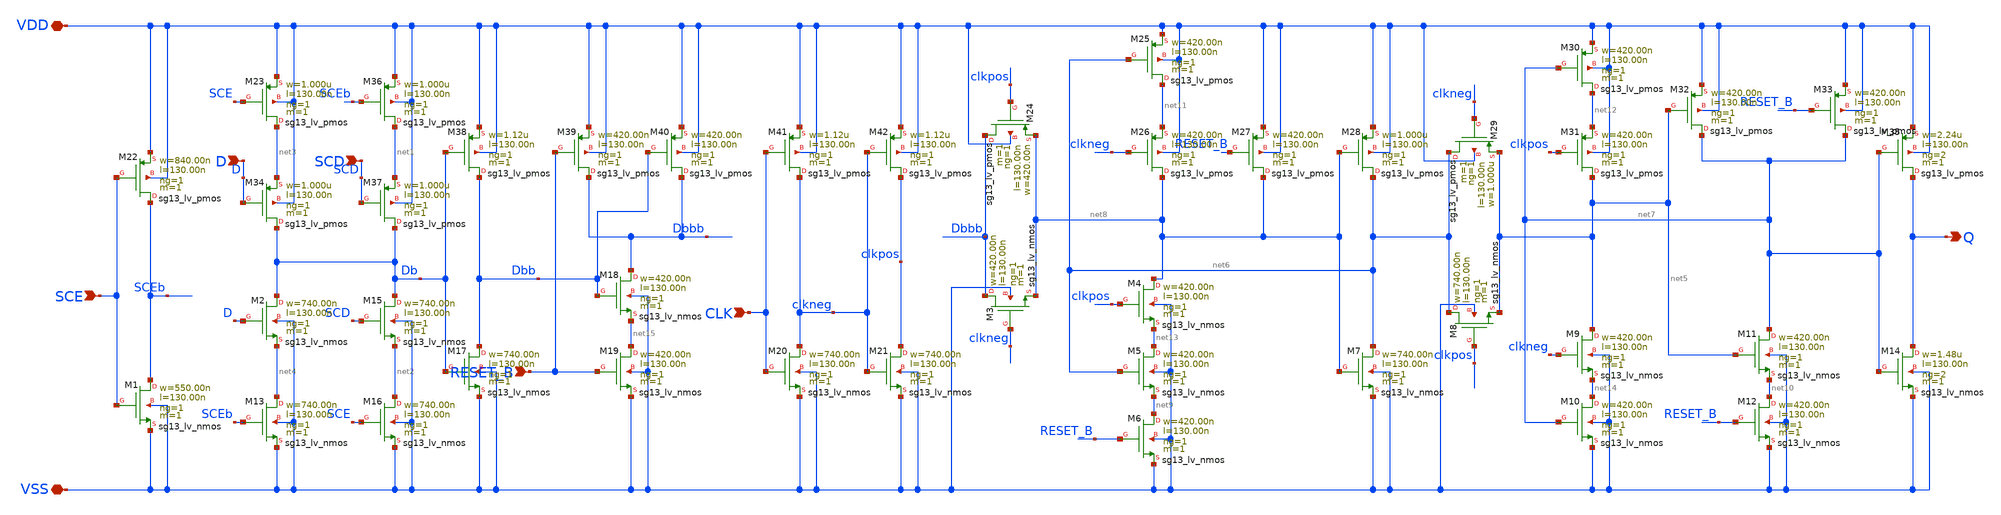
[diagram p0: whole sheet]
** sch_path: ihp-sg13g2/libs.tech/xschem/sg13g2_stdcells/sg13g2_sdfrbpq_2.sch
**.subckt sg13g2_sdfrbpq_2 Q CLK D RESET_B SCD SCE VDD VSS
*.opin Q
*.ipin CLK
*.ipin D
*.ipin RESET_B
*.ipin SCD
*.ipin SCE
*.iopin VDD
*.iopin VSS
XM1 SCEb SCE VSS VSS sg13_lv_nmos w=550.00n l=130.00n ng=1 m=1 mm_ok=1
XM2 Db D net4 VSS sg13_lv_nmos w=740.00n l=130.00n ng=1 m=1 mm_ok=1
XM3 Dbbb clkneg net8 VSS sg13_lv_nmos w=420.00n l=130.00n ng=1 m=1 mm_ok=1
XM4 net8 clkpos net13 VSS sg13_lv_nmos w=420.00n l=130.00n ng=1 m=1 mm_ok=1
XM5 net13 net6 net9 VSS sg13_lv_nmos w=420.00n l=130.00n ng=1 m=1 mm_ok=1
XM6 net9 RESET_B VSS VSS sg13_lv_nmos w=420.00n l=130.00n ng=1 m=1 mm_ok=1
XM7 net6 net8 VSS VSS sg13_lv_nmos w=740.00n l=130.00n ng=1 m=1 mm_ok=1
XM8 net6 clkpos net5 VSS sg13_lv_nmos w=740.00n l=130.00n ng=1 m=1 mm_ok=1
XM9 net5 clkneg net14 VSS sg13_lv_nmos w=420.00n l=130.00n ng=1 m=1 mm_ok=1
XM10 net14 net7 VSS VSS sg13_lv_nmos w=420.00n l=130.00n ng=1 m=1 mm_ok=1
XM11 net7 net5 net10 VSS sg13_lv_nmos w=420.00n l=130.00n ng=1 m=1 mm_ok=1
XM12 net10 RESET_B VSS VSS sg13_lv_nmos w=420.00n l=130.00n ng=1 m=1 mm_ok=1
XM13 net4 SCEb VSS VSS sg13_lv_nmos w=740.00n l=130.00n ng=1 m=1 mm_ok=1
XM14 Q net7 VSS VSS sg13_lv_nmos w=1.48u l=130.00n ng=2 m=1 mm_ok=1
XM15 Db SCD net2 VSS sg13_lv_nmos w=740.00n l=130.00n ng=1 m=1 mm_ok=1
XM16 net2 SCE VSS VSS sg13_lv_nmos w=740.00n l=130.00n ng=1 m=1 mm_ok=1
XM17 Dbb Db VSS VSS sg13_lv_nmos w=740.00n l=130.00n ng=1 m=1 mm_ok=1
XM18 Dbbb Dbb net15 VSS sg13_lv_nmos w=420.00n l=130.00n ng=1 m=1 mm_ok=1
XM19 net15 RESET_B VSS VSS sg13_lv_nmos w=420.00n l=130.00n ng=1 m=1 mm_ok=1
XM20 clkneg CLK VSS VSS sg13_lv_nmos w=740.00n l=130.00n ng=1 m=1 mm_ok=1
XM21 clkpos clkneg VSS VSS sg13_lv_nmos w=740.00n l=130.00n ng=1 m=1 mm_ok=1
XM22 SCEb SCE VDD VDD sg13_lv_pmos w=840.00n l=130.00n ng=1 m=1 mm_ok=1
XM23 net3 SCE VDD VDD sg13_lv_pmos w=1.000u l=130.00n ng=1 m=1 mm_ok=1
XM24 Dbbb clkpos net8 VDD sg13_lv_pmos w=420.00n l=130.00n ng=1 m=1 mm_ok=1
XM25 net11 net6 VDD VDD sg13_lv_pmos w=420.00n l=130.00n ng=1 m=1 mm_ok=1
XM26 net8 clkneg net11 VDD sg13_lv_pmos w=420.00n l=130.00n ng=1 m=1 mm_ok=1
XM27 net8 RESET_B VDD VDD sg13_lv_pmos w=420.00n l=130.00n ng=1 m=1 mm_ok=1
XM28 net6 net8 VDD VDD sg13_lv_pmos w=1.000u l=130.00n ng=1 m=1 mm_ok=1
XM29 net6 clkneg net5 VDD sg13_lv_pmos w=1.000u l=130.00n ng=1 m=1 mm_ok=1
XM30 net12 net7 VDD VDD sg13_lv_pmos w=420.00n l=130.00n ng=1 m=1 mm_ok=1
XM31 net5 clkpos net12 VDD sg13_lv_pmos w=420.00n l=130.00n ng=1 m=1 mm_ok=1
XM32 net7 net5 VDD VDD sg13_lv_pmos w=420.00n l=130.00n ng=1 m=1 mm_ok=1
XM33 net7 RESET_B VDD VDD sg13_lv_pmos w=420.00n l=130.00n ng=1 m=1 mm_ok=1
XM34 Db D net3 VDD sg13_lv_pmos w=1.000u l=130.00n ng=1 m=1 mm_ok=1
XM35 Q net7 VDD VDD sg13_lv_pmos w=2.24u l=130.00n ng=2 m=1 mm_ok=1
XM36 net1 SCEb VDD VDD sg13_lv_pmos w=1.000u l=130.00n ng=1 m=1 mm_ok=1
XM37 Db SCD net1 VDD sg13_lv_pmos w=1.000u l=130.00n ng=1 m=1 mm_ok=1
XM38 Dbb Db VDD VDD sg13_lv_pmos w=1.12u l=130.00n ng=1 m=1 mm_ok=1
XM39 Dbbb RESET_B VDD VDD sg13_lv_pmos w=420.00n l=130.00n ng=1 m=1 mm_ok=1
XM40 Dbbb Dbb VDD VDD sg13_lv_pmos w=420.00n l=130.00n ng=1 m=1 mm_ok=1
XM41 clkneg CLK VDD VDD sg13_lv_pmos w=1.12u l=130.00n ng=1 m=1 mm_ok=1
XM42 clkpos clkneg VDD VDD sg13_lv_pmos w=1.12u l=130.00n ng=1 m=1 mm_ok=1
**.ends
.end
